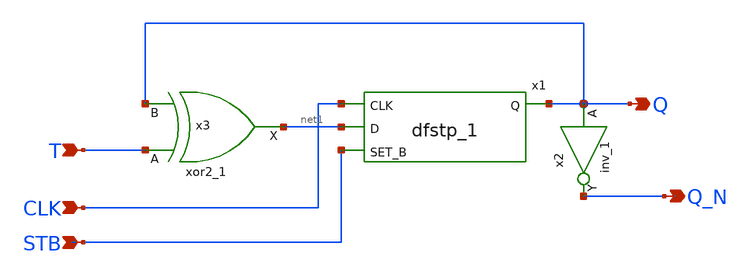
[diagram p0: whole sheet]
** sch_path: xschem/T_flip_flop/asyn_st_tff.sch
**.subckt asyn_st_tff T CLK Q STB Q_N
*.ipin T
*.ipin CLK
*.opin Q
*.ipin STB
*.opin Q_N
x3 T Q GND GND VDD VDD net1 sky130_fd_sc_lp__xor2_1
x2 Q GND GND VDD VDD Q_N sky130_fd_sc_lp__inv_1
x1 CLK net1 STB GND GND VDD VDD Q sky130_fd_sc_lp__dfstp_1
**.ends
.end
